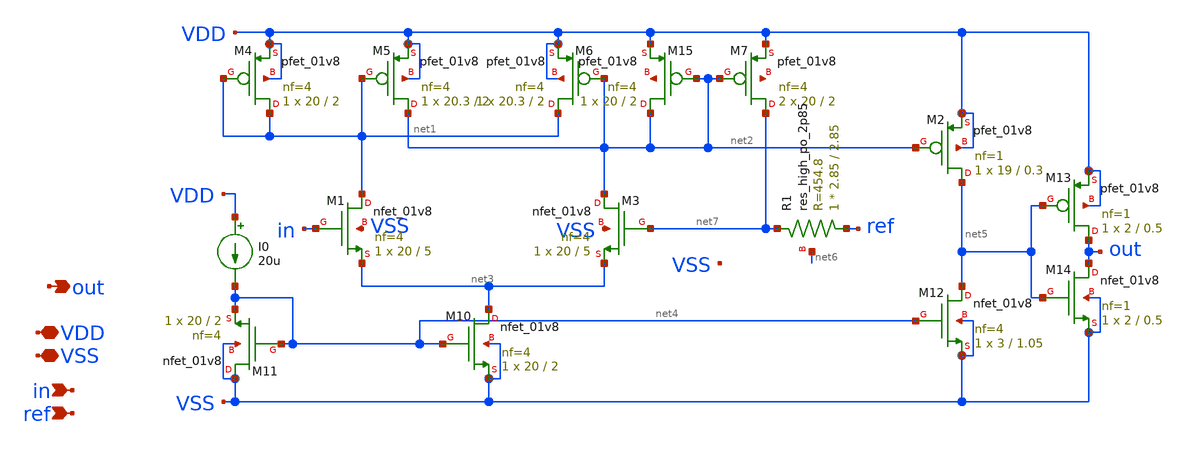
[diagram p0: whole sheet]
** sch_path: xschem/src/comparator2/sorta_working_slow.sch
**.subckt sorta_working_slow VDD in out VSS ref
*.iopin VDD
*.ipin in
*.opin out
*.iopin VSS
*.ipin ref
XM4 net1 net1 VDD VDD sky130_fd_pr__pfet_01v8 L=2 W=20 nf=4 ad='int((nf+1)/2) * W/nf * 0.29' as='int((nf+2)/2) * W/nf * 0.29'
+ pd='2*int((nf+1)/2) * (W/nf + 0.29)' ps='2*int((nf+2)/2) * (W/nf + 0.29)' nrd='0.29 / W' nrs='0.29 / W'
+ sa=0 sb=0 sd=0 mult=1 m=1
XM5 net2 net1 VDD VDD sky130_fd_pr__pfet_01v8 L=2 W=20.3 nf=4 ad='int((nf+1)/2) * W/nf * 0.29' as='int((nf+2)/2) * W/nf * 0.29'
+ pd='2*int((nf+1)/2) * (W/nf + 0.29)' ps='2*int((nf+2)/2) * (W/nf + 0.29)' nrd='0.29 / W' nrs='0.29 / W'
+ sa=0 sb=0 sd=0 mult=1 m=1
XM6 net1 net2 VDD VDD sky130_fd_pr__pfet_01v8 L=2 W=20.3 nf=4 ad='int((nf+1)/2) * W/nf * 0.29' as='int((nf+2)/2) * W/nf * 0.29'
+ pd='2*int((nf+1)/2) * (W/nf + 0.29)' ps='2*int((nf+2)/2) * (W/nf + 0.29)' nrd='0.29 / W' nrs='0.29 / W'
+ sa=0 sb=0 sd=0 mult=1 m=1
XM7 net7 net2 VDD net8 sky130_fd_pr__pfet_01v8 L=2 W=20 nf=4 ad='int((nf+1)/2) * W/nf * 0.29' as='int((nf+2)/2) * W/nf * 0.29'
+ pd='2*int((nf+1)/2) * (W/nf + 0.29)' ps='2*int((nf+2)/2) * (W/nf + 0.29)' nrd='0.29 / W' nrs='0.29 / W'
+ sa=0 sb=0 sd=0 mult=2 m=2
XM10 net3 net4 VSS VSS sky130_fd_pr__nfet_01v8 L=2 W=20 nf=4 ad='int((nf+1)/2) * W/nf * 0.29' as='int((nf+2)/2) * W/nf * 0.29'
+ pd='2*int((nf+1)/2) * (W/nf + 0.29)' ps='2*int((nf+2)/2) * (W/nf + 0.29)' nrd='0.29 / W' nrs='0.29 / W'
+ sa=0 sb=0 sd=0 mult=1 m=1
XM11 VSS net4 net4 VSS sky130_fd_pr__nfet_01v8 L=2 W=20 nf=4 ad='int((nf+1)/2) * W/nf * 0.29' as='int((nf+2)/2) * W/nf * 0.29'
+ pd='2*int((nf+1)/2) * (W/nf + 0.29)' ps='2*int((nf+2)/2) * (W/nf + 0.29)' nrd='0.29 / W' nrs='0.29 / W'
+ sa=0 sb=0 sd=0 mult=1 m=1
XM12 net5 net4 VSS VSS sky130_fd_pr__nfet_01v8 L=1.05 W=3 nf=4 ad='int((nf+1)/2) * W/nf * 0.29' as='int((nf+2)/2) * W/nf * 0.29'
+ pd='2*int((nf+1)/2) * (W/nf + 0.29)' ps='2*int((nf+2)/2) * (W/nf + 0.29)' nrd='0.29 / W' nrs='0.29 / W'
+ sa=0 sb=0 sd=0 mult=1 m=1
XM13 out net5 VDD VDD sky130_fd_pr__pfet_01v8 L=0.5 W=2 nf=1 ad='int((nf+1)/2) * W/nf * 0.29' as='int((nf+2)/2) * W/nf * 0.29'
+ pd='2*int((nf+1)/2) * (W/nf + 0.29)' ps='2*int((nf+2)/2) * (W/nf + 0.29)' nrd='0.29 / W' nrs='0.29 / W'
+ sa=0 sb=0 sd=0 mult=1 m=1
XM14 out net5 VSS VSS sky130_fd_pr__nfet_01v8 L=0.5 W=2 nf=1 ad='int((nf+1)/2) * W/nf * 0.29' as='int((nf+2)/2) * W/nf * 0.29'
+ pd='2*int((nf+1)/2) * (W/nf + 0.29)' ps='2*int((nf+2)/2) * (W/nf + 0.29)' nrd='0.29 / W' nrs='0.29 / W'
+ sa=0 sb=0 sd=0 mult=1 m=1
XM15 net2 net2 VDD net9 sky130_fd_pr__pfet_01v8 L=2 W=20 nf=4 ad='int((nf+1)/2) * W/nf * 0.29' as='int((nf+2)/2) * W/nf * 0.29'
+ pd='2*int((nf+1)/2) * (W/nf + 0.29)' ps='2*int((nf+2)/2) * (W/nf + 0.29)' nrd='0.29 / W' nrs='0.29 / W'
+ sa=0 sb=0 sd=0 mult=1 m=1
I0 VDD net4 20u
XM2 net5 net2 VDD VDD sky130_fd_pr__pfet_01v8 L=0.3 W=19 nf=1 ad='int((nf+1)/2) * W/nf * 0.29' as='int((nf+2)/2) * W/nf * 0.29'
+ pd='2*int((nf+1)/2) * (W/nf + 0.29)' ps='2*int((nf+2)/2) * (W/nf + 0.29)' nrd='0.29 / W' nrs='0.29 / W'
+ sa=0 sb=0 sd=0 mult=1 m=1
XM1 net1 in net3 VSS sky130_fd_pr__nfet_01v8 L=5 W=20 nf=4 ad='int((nf+1)/2) * W/nf * 0.29' as='int((nf+2)/2) * W/nf * 0.29'
+ pd='2*int((nf+1)/2) * (W/nf + 0.29)' ps='2*int((nf+2)/2) * (W/nf + 0.29)' nrd='0.29 / W' nrs='0.29 / W'
+ sa=0 sb=0 sd=0 mult=1 m=1
XM3 net2 net7 net3 VSS sky130_fd_pr__nfet_01v8 L=5 W=20 nf=4 ad='int((nf+1)/2) * W/nf * 0.29' as='int((nf+2)/2) * W/nf * 0.29'
+ pd='2*int((nf+1)/2) * (W/nf + 0.29)' ps='2*int((nf+2)/2) * (W/nf + 0.29)' nrd='0.29 / W' nrs='0.29 / W'
+ sa=0 sb=0 sd=0 mult=1 m=1
XR1 ref net7 net6 sky130_fd_pr__res_high_po_2p85 L=2.85 mult=1 m=1
**.ends
.end
